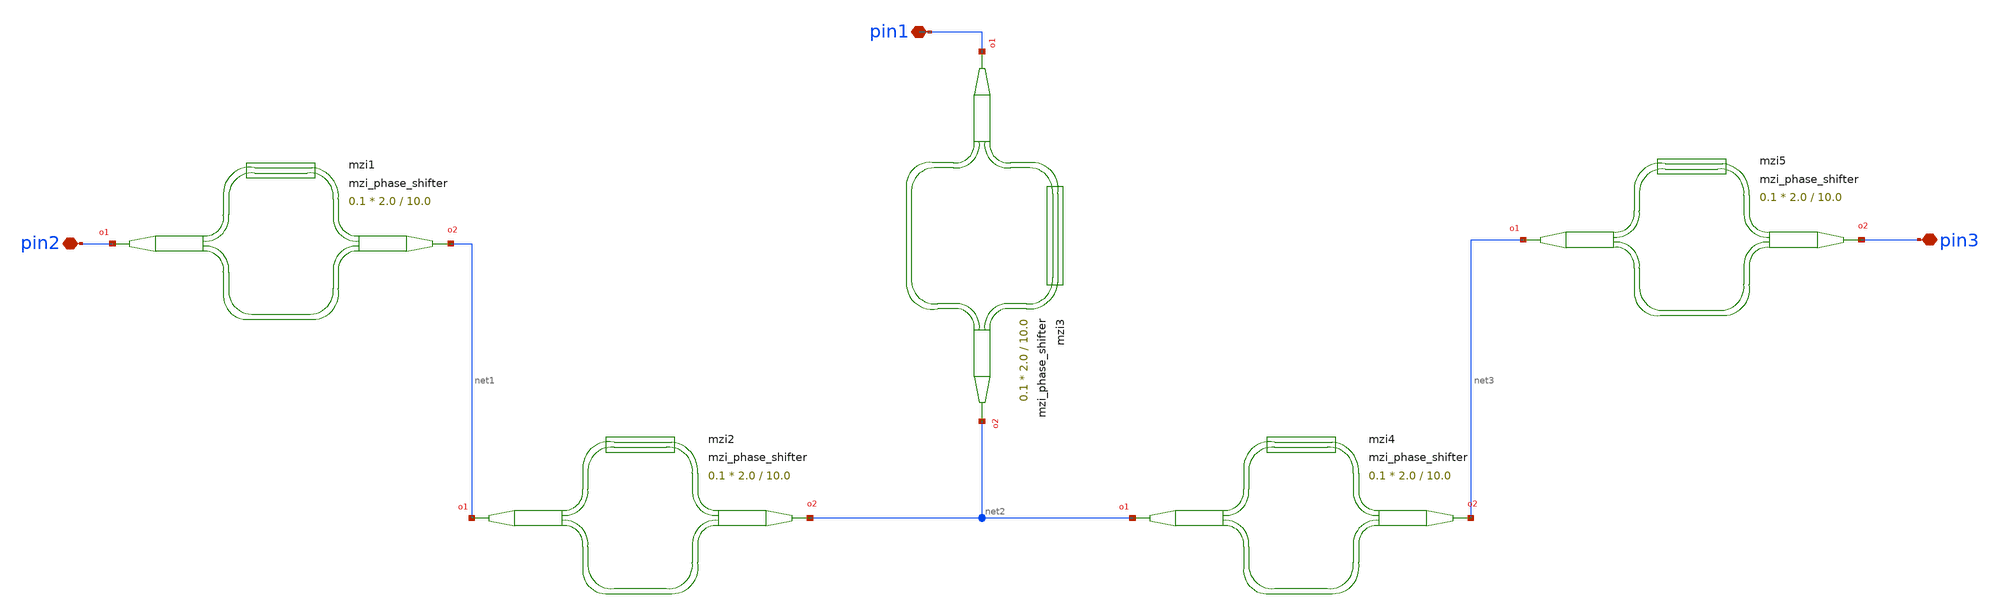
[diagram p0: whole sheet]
** sch_path: cells/xschem/tests/test_mzi_phase_shifter.sch
* SPDX-FileCopyrightText: 2023 Mabrains Company
* Licensed under the GNU GENERAL PUBLIC License, Version 3.0 (the "License");
* you may not use this file except in compliance with the License.
* GNU GENERAL PUBLIC LICENSE
* Version 3, 29 June 2007
* This program is free software: you can redistribute it and/or modify
* it under the terms of the GNU General Public License as published
* by the Free Software Foundation, either 3 of the License, or
* (at your option) any later version.
* This program is distributed in the hope that it will be useful,
* but WITHOUT ANY WARRANTY; without even the implied warranty of
* MERCHANTABILITY or FITNESS FOR A PARTICULAR PURPOSE.  See the
* GNU General Public License for more details.
* You should have received a copy of the GNU General Public License
* along with this program.  If not, see <https://www.gnu.org/licenses/>.
* SPDX-License-Identifier: GPL-3.0
**.subckt test_mzi_phase_shifter pin2 pin1 pin3
*.iopin pin2
*.iopin pin1
*.iopin pin3
Pmzi1 pin2 net1 mzi_phase_shifter delta_length=10.0 length_y=2.0 length_x=0.1
Pmzi2 net1 net2 mzi_phase_shifter delta_length=10.0 length_y=2.0 length_x=0.1
Pmzi3 pin1 net2 mzi_phase_shifter delta_length=10.0 length_y=2.0 length_x=0.1
Pmzi4 net2 net3 mzi_phase_shifter delta_length=10.0 length_y=2.0 length_x=0.1
Pmzi5 net3 pin3 mzi_phase_shifter delta_length=10.0 length_y=2.0 length_x=0.1
**.ends
.end
